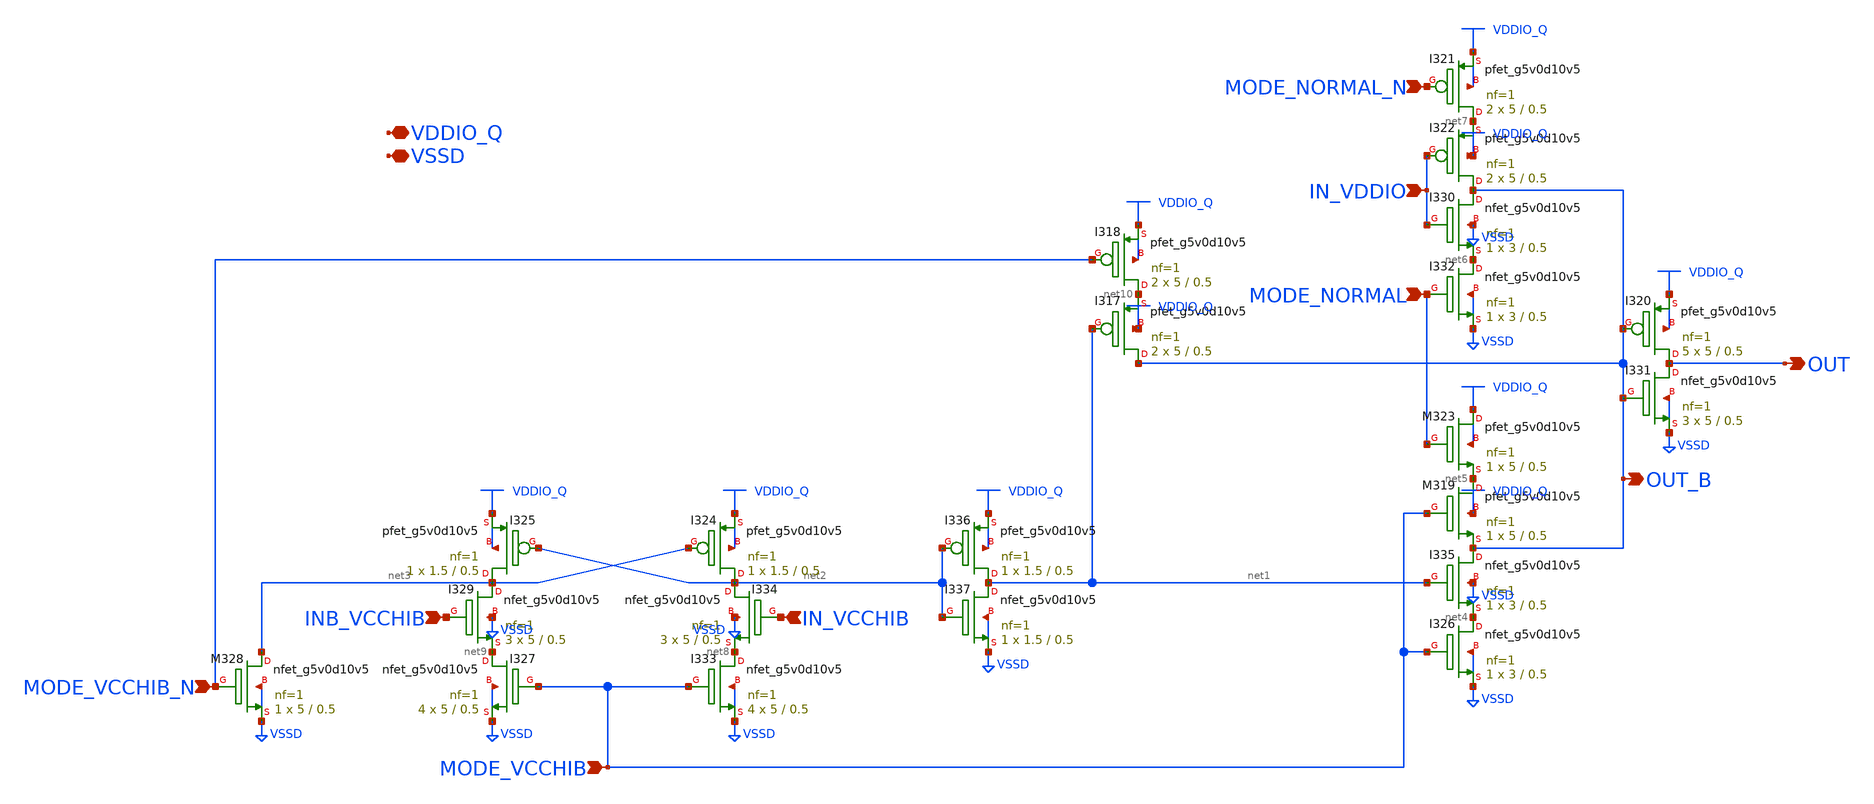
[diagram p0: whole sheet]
** sch_path: gpiov2_ipath_hvls.sch
* Copyright 2023 David Mitchell Bailey
* Licensed under the Apache License, Version 2.0 (the "License");
* you may not use this file except in compliance with the License.
* You may obtain a copy of the License at
* https://www.apache.org/licenses/LICENSE-2.0
* Unless required by applicable law or agreed to in writing, software
* distributed under the License is distributed on an "AS IS" BASIS,
* WITHOUT WARRANTIES OR CONDITIONS OF ANY KIND, either express or implied.
* See the License for the specific language governing permissions and
* limitations under the License.
**.subckt gpiov2_ipath_hvls MODE_VCCHIB_N VDDIO_Q VSSD OUT MODE_NORMAL_N IN_VDDIO MODE_NORMAL
*+ INB_VCCHIB IN_VCCHIB MODE_VCCHIB OUT_B
*.ipin MODE_VCCHIB_N
*.iopin VDDIO_Q
*.iopin VSSD
*.opin OUT
*.ipin MODE_NORMAL_N
*.ipin IN_VDDIO
*.ipin MODE_NORMAL
*.ipin INB_VCCHIB
*.ipin IN_VCCHIB
*.ipin MODE_VCCHIB
*.opin OUT_B
XI326 net4 MODE_VCCHIB VSSD VSSD sky130_fd_pr__nfet_g5v0d10v5 L=0.5 W=3 nf=1 ad='int((nf+1)/2) * W/nf * 0.29'
+ as='int((nf+2)/2) * W/nf * 0.29' pd='2*int((nf+1)/2) * (W/nf + 0.29)' ps='2*int((nf+2)/2) * (W/nf + 0.29)'
+ nrd='0.29 / W' nrs='0.29 / W' sa=0 sb=0 sd=0 mult=1 m=1
XI335 OUT_B net1 net4 VSSD sky130_fd_pr__nfet_g5v0d10v5 L=0.5 W=3 nf=1 ad='int((nf+1)/2) * W/nf * 0.29'
+ as='int((nf+2)/2) * W/nf * 0.29' pd='2*int((nf+1)/2) * (W/nf + 0.29)' ps='2*int((nf+2)/2) * (W/nf + 0.29)'
+ nrd='0.29 / W' nrs='0.29 / W' sa=0 sb=0 sd=0 mult=1 m=1
XM319 net5 MODE_VCCHIB OUT_B VDDIO_Q sky130_fd_pr__pfet_g5v0d10v5 L=0.5 W=5 nf=1 ad='int((nf+1)/2) * W/nf * 0.29'
+ as='int((nf+2)/2) * W/nf * 0.29' pd='2*int((nf+1)/2) * (W/nf + 0.29)' ps='2*int((nf+2)/2) * (W/nf + 0.29)'
+ nrd='0.29 / W' nrs='0.29 / W' sa=0 sb=0 sd=0 mult=1 m=1
XM323 VDDIO_Q MODE_NORMAL net5 VDDIO_Q sky130_fd_pr__pfet_g5v0d10v5 L=0.5 W=5 nf=1 ad='int((nf+1)/2) * W/nf * 0.29'
+ as='int((nf+2)/2) * W/nf * 0.29' pd='2*int((nf+1)/2) * (W/nf + 0.29)' ps='2*int((nf+2)/2) * (W/nf + 0.29)'
+ nrd='0.29 / W' nrs='0.29 / W' sa=0 sb=0 sd=0 mult=1 m=1
XI332 net6 MODE_NORMAL VSSD VSSD sky130_fd_pr__nfet_g5v0d10v5 L=0.5 W=3 nf=1 ad='int((nf+1)/2) * W/nf * 0.29'
+ as='int((nf+2)/2) * W/nf * 0.29' pd='2*int((nf+1)/2) * (W/nf + 0.29)' ps='2*int((nf+2)/2) * (W/nf + 0.29)'
+ nrd='0.29 / W' nrs='0.29 / W' sa=0 sb=0 sd=0 mult=1 m=1
XI330 OUT_B IN_VDDIO net6 VSSD sky130_fd_pr__nfet_g5v0d10v5 L=0.5 W=3 nf=1 ad='int((nf+1)/2) * W/nf * 0.29'
+ as='int((nf+2)/2) * W/nf * 0.29' pd='2*int((nf+1)/2) * (W/nf + 0.29)' ps='2*int((nf+2)/2) * (W/nf + 0.29)'
+ nrd='0.29 / W' nrs='0.29 / W' sa=0 sb=0 sd=0 mult=1 m=1
XI322 OUT_B IN_VDDIO net7 VDDIO_Q sky130_fd_pr__pfet_g5v0d10v5 L=0.5 W=5 nf=1 ad='int((nf+1)/2) * W/nf * 0.29'
+ as='int((nf+2)/2) * W/nf * 0.29' pd='2*int((nf+1)/2) * (W/nf + 0.29)' ps='2*int((nf+2)/2) * (W/nf + 0.29)'
+ nrd='0.29 / W' nrs='0.29 / W' sa=0 sb=0 sd=0 mult=2 m=2
XI321 net7 MODE_NORMAL_N VDDIO_Q VDDIO_Q sky130_fd_pr__pfet_g5v0d10v5 L=0.5 W=5 nf=1 ad='int((nf+1)/2) * W/nf * 0.29'
+ as='int((nf+2)/2) * W/nf * 0.29' pd='2*int((nf+1)/2) * (W/nf + 0.29)' ps='2*int((nf+2)/2) * (W/nf + 0.29)'
+ nrd='0.29 / W' nrs='0.29 / W' sa=0 sb=0 sd=0 mult=2 m=2
XI337 net1 net2 VSSD VSSD sky130_fd_pr__nfet_g5v0d10v5 L=0.5 W=1.5 nf=1 ad='int((nf+1)/2) * W/nf * 0.29'
+ as='int((nf+2)/2) * W/nf * 0.29' pd='2*int((nf+1)/2) * (W/nf + 0.29)' ps='2*int((nf+2)/2) * (W/nf + 0.29)'
+ nrd='0.29 / W' nrs='0.29 / W' sa=0 sb=0 sd=0 mult=1 m=1
XI336 net1 net2 VDDIO_Q VDDIO_Q sky130_fd_pr__pfet_g5v0d10v5 L=0.5 W=1.5 nf=1 ad='int((nf+1)/2) * W/nf * 0.29'
+ as='int((nf+2)/2) * W/nf * 0.29' pd='2*int((nf+1)/2) * (W/nf + 0.29)' ps='2*int((nf+2)/2) * (W/nf + 0.29)'
+ nrd='0.29 / W' nrs='0.29 / W' sa=0 sb=0 sd=0 mult=1 m=1
XI333 net8 MODE_VCCHIB VSSD VSSD sky130_fd_pr__nfet_g5v0d10v5 L=0.5 W=5 nf=1 ad='int((nf+1)/2) * W/nf * 0.29'
+ as='int((nf+2)/2) * W/nf * 0.29' pd='2*int((nf+1)/2) * (W/nf + 0.29)' ps='2*int((nf+2)/2) * (W/nf + 0.29)'
+ nrd='0.29 / W' nrs='0.29 / W' sa=0 sb=0 sd=0 mult=4 m=4
XI334 net2 IN_VCCHIB net8 VSSD sky130_fd_pr__nfet_g5v0d10v5 L=0.5 W=5 nf=1 ad='int((nf+1)/2) * W/nf * 0.29'
+ as='int((nf+2)/2) * W/nf * 0.29' pd='2*int((nf+1)/2) * (W/nf + 0.29)' ps='2*int((nf+2)/2) * (W/nf + 0.29)'
+ nrd='0.29 / W' nrs='0.29 / W' sa=0 sb=0 sd=0 mult=3 m=3
XI327 net9 MODE_VCCHIB VSSD VSSD sky130_fd_pr__nfet_g5v0d10v5 L=0.5 W=5 nf=1 ad='int((nf+1)/2) * W/nf * 0.29'
+ as='int((nf+2)/2) * W/nf * 0.29' pd='2*int((nf+1)/2) * (W/nf + 0.29)' ps='2*int((nf+2)/2) * (W/nf + 0.29)'
+ nrd='0.29 / W' nrs='0.29 / W' sa=0 sb=0 sd=0 mult=4 m=4
XI329 net3 INB_VCCHIB net9 VSSD sky130_fd_pr__nfet_g5v0d10v5 L=0.5 W=5 nf=1 ad='int((nf+1)/2) * W/nf * 0.29'
+ as='int((nf+2)/2) * W/nf * 0.29' pd='2*int((nf+1)/2) * (W/nf + 0.29)' ps='2*int((nf+2)/2) * (W/nf + 0.29)'
+ nrd='0.29 / W' nrs='0.29 / W' sa=0 sb=0 sd=0 mult=3 m=3
XI324 net2 net3 VDDIO_Q VDDIO_Q sky130_fd_pr__pfet_g5v0d10v5 L=0.5 W=1.5 nf=1 ad='int((nf+1)/2) * W/nf * 0.29'
+ as='int((nf+2)/2) * W/nf * 0.29' pd='2*int((nf+1)/2) * (W/nf + 0.29)' ps='2*int((nf+2)/2) * (W/nf + 0.29)'
+ nrd='0.29 / W' nrs='0.29 / W' sa=0 sb=0 sd=0 mult=1 m=1
XI325 net3 net2 VDDIO_Q VDDIO_Q sky130_fd_pr__pfet_g5v0d10v5 L=0.5 W=1.5 nf=1 ad='int((nf+1)/2) * W/nf * 0.29'
+ as='int((nf+2)/2) * W/nf * 0.29' pd='2*int((nf+1)/2) * (W/nf + 0.29)' ps='2*int((nf+2)/2) * (W/nf + 0.29)'
+ nrd='0.29 / W' nrs='0.29 / W' sa=0 sb=0 sd=0 mult=1 m=1
XM328 net3 MODE_VCCHIB_N VSSD VSSD sky130_fd_pr__nfet_g5v0d10v5 L=0.5 W=5 nf=1 ad='int((nf+1)/2) * W/nf * 0.29'
+ as='int((nf+2)/2) * W/nf * 0.29' pd='2*int((nf+1)/2) * (W/nf + 0.29)' ps='2*int((nf+2)/2) * (W/nf + 0.29)'
+ nrd='0.29 / W' nrs='0.29 / W' sa=0 sb=0 sd=0 mult=1 m=1
XI317 OUT_B net1 net10 VDDIO_Q sky130_fd_pr__pfet_g5v0d10v5 L=0.5 W=5 nf=1 ad='int((nf+1)/2) * W/nf * 0.29'
+ as='int((nf+2)/2) * W/nf * 0.29' pd='2*int((nf+1)/2) * (W/nf + 0.29)' ps='2*int((nf+2)/2) * (W/nf + 0.29)'
+ nrd='0.29 / W' nrs='0.29 / W' sa=0 sb=0 sd=0 mult=2 m=2
XI318 net10 MODE_VCCHIB_N VDDIO_Q VDDIO_Q sky130_fd_pr__pfet_g5v0d10v5 L=0.5 W=5 nf=1 ad='int((nf+1)/2) * W/nf * 0.29'
+ as='int((nf+2)/2) * W/nf * 0.29' pd='2*int((nf+1)/2) * (W/nf + 0.29)' ps='2*int((nf+2)/2) * (W/nf + 0.29)'
+ nrd='0.29 / W' nrs='0.29 / W' sa=0 sb=0 sd=0 mult=2 m=2
XI331 OUT OUT_B VSSD VSSD sky130_fd_pr__nfet_g5v0d10v5 L=0.5 W=5 nf=1 ad='int((nf+1)/2) * W/nf * 0.29'
+ as='int((nf+2)/2) * W/nf * 0.29' pd='2*int((nf+1)/2) * (W/nf + 0.29)' ps='2*int((nf+2)/2) * (W/nf + 0.29)'
+ nrd='0.29 / W' nrs='0.29 / W' sa=0 sb=0 sd=0 mult=3 m=3
XI320 OUT OUT_B VDDIO_Q VDDIO_Q sky130_fd_pr__pfet_g5v0d10v5 L=0.5 W=5 nf=1 ad='int((nf+1)/2) * W/nf * 0.29'
+ as='int((nf+2)/2) * W/nf * 0.29' pd='2*int((nf+1)/2) * (W/nf + 0.29)' ps='2*int((nf+2)/2) * (W/nf + 0.29)'
+ nrd='0.29 / W' nrs='0.29 / W' sa=0 sb=0 sd=0 mult=5 m=5
**.ends
.end
